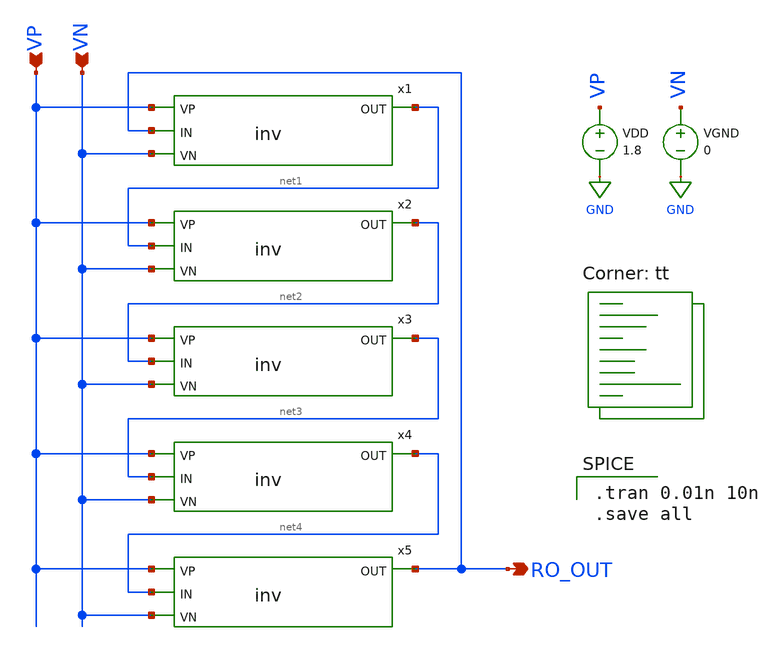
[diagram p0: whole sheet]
** sch_path: Mixed-Signal TRNG/xschem/ro.sch
**.subckt ro RO_OUT VP VN
*.opin RO_OUT
*.ipin VP
*.ipin VN
x1 VP RO_OUT net1 VN inv
x2 VP net1 net2 VN inv
x3 VP net2 net3 VN inv
x4 VP net3 net4 VN inv
x5 VP net4 RO_OUT VN inv
VDD VP GND 1.8
VGND VN GND 0
**** begin user architecture code

.tran 0.01n 10n
.save all

.lib $::SKYWATER_MODELS/sky130.lib.spice tt
**** end user architecture code
**.ends

* expanding   symbol:  /home/madvlsi/Desktop/Mixed-Signal TRNG/xschem/inv.sym # of pins=4
** sym_path: Mixed-Signal TRNG/xschem/inv.sym
** sch_path: Mixed-Signal TRNG/xschem/inv.sch
.subckt inv VP IN OUT VN
*.ipin IN
*.opin OUT
*.ipin VP
*.ipin VN
XM1 OUT IN VN VN sky130_fd_pr__nfet_01v8 L=0.15 W=2 nf=1 ad='int((nf+1)/2) * W/nf * 0.29' as='int((nf+2)/2) * W/nf * 0.29'
+ pd='2*int((nf+1)/2) * (W/nf + 0.29)' ps='2*int((nf+2)/2) * (W/nf + 0.29)' nrd='0.29 / W' nrs='0.29 / W'
+ sa=0 sb=0 sd=0 mult=1 m=1
XM2 OUT IN VP VP sky130_fd_pr__pfet_01v8 L=0.15 W=4 nf=1 ad='int((nf+1)/2) * W/nf * 0.29' as='int((nf+2)/2) * W/nf * 0.29'
+ pd='2*int((nf+1)/2) * (W/nf + 0.29)' ps='2*int((nf+2)/2) * (W/nf + 0.29)' nrd='0.29 / W' nrs='0.29 / W'
+ sa=0 sb=0 sd=0 mult=1 m=1
.ends

.GLOBAL GND
.end
